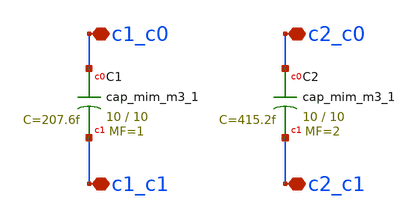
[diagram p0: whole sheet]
** sch_path: xschem/caps.sch
**.subckt caps c1_c0 c1_c1 c2_c0 c2_c1
*.iopin c1_c0
*.iopin c1_c1
*.iopin c2_c0
*.iopin c2_c1
XC1 c1_c0 c1_c1 sky130_fd_pr__cap_mim_m3_1 W=10 L=10 MF=1 m=1
XC2 c2_c0 c2_c1 sky130_fd_pr__cap_mim_m3_1 W=10 L=10 MF=2 m=2
**.ends
.end
